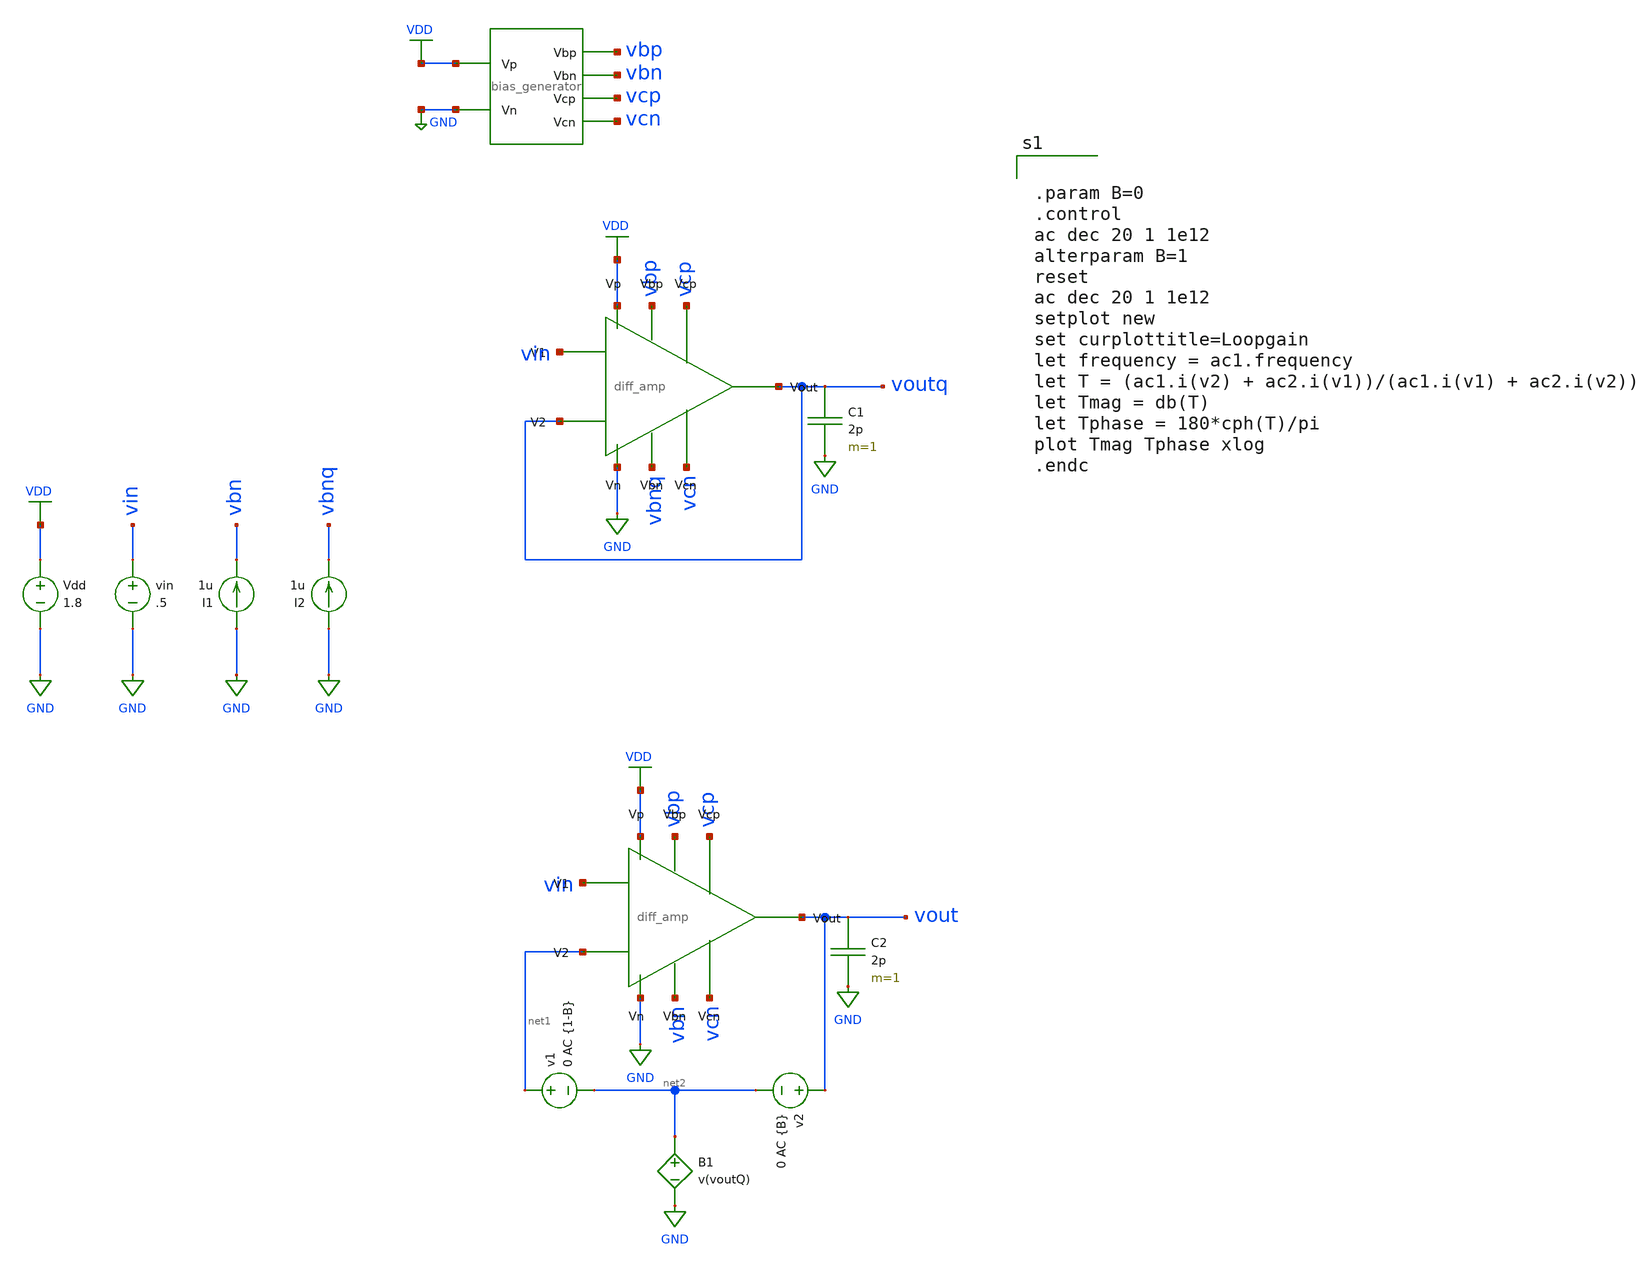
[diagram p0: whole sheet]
** sch_path: mini_proj_3/schematic/diff_loopgain.sch
**.subckt diff_loopgain
Vdd VDD GND 1.8
vin vin GND .5
I1 GND vbn 1u
X1 VDD GND vbp vbn vcp vcn bias_generator
X3 VDD GND vbp vbnq vcp vcn vin voutq voutq diff_amp
C1 voutq GND 2p m=1
X2 VDD GND vbp vbn vcp vcn vin net1 vout diff_amp
C2 vout GND 2p m=1
I2 GND vbnq 1u
v1 net1 net2 0 AC {1-B}
v2 vout net2 0 AC {B}
B1 net2 GND V=v(voutQ)
**** begin user architecture code

.option wnflag=1
.lib ~/skywater/skywater-pdk/libraries/sky130_fd_pr_ngspice/latest/models/sky130.lib.spice tt



.param B=0
.control
ac dec 20 1 1e12
alterparam B=1
reset
ac dec 20 1 1e12
setplot new
set curplottitle=Loopgain
let frequency = ac1.frequency
let T = (ac1.i(v2) + ac2.i(v1))/(ac1.i(v1) + ac2.i(v2))
let Tmag = db(T)
let Tphase = 180*cph(T)/pi
plot Tmag Tphase xlog
.endc

**** end user architecture code
**.ends
.GLOBAL GND
.GLOBAL VDD
.end
